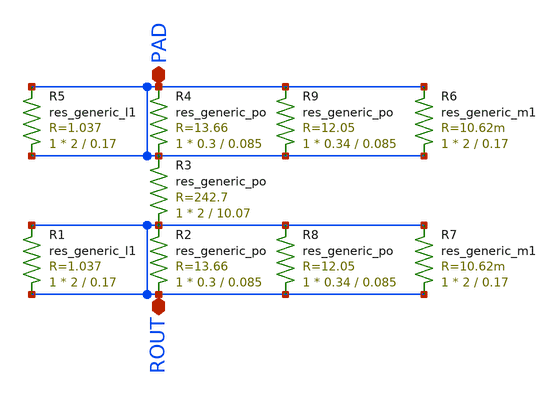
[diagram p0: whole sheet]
** sch_path: res250only_small.sch
* Copyright 2023 David Mitchell Bailey
* Licensed under the Apache License, Version 2.0 (the "License");
* you may not use this file except in compliance with the License.
* You may obtain a copy of the License at
* https://www.apache.org/licenses/LICENSE-2.0
* Unless required by applicable law or agreed to in writing, software
* distributed under the License is distributed on an "AS IS" BASIS,
* WITHOUT WARRANTIES OR CONDITIONS OF ANY KIND, either express or implied.
* See the License for the specific language governing permissions and
* limitations under the License.
**.subckt res250only_small PAD ROUT
*.iopin PAD
*.iopin ROUT
XR2 ROUT ROUT sky130_fd_pr__res_generic_po W=0.3 L=0.085 m=1
XR3 ROUT PAD sky130_fd_pr__res_generic_po W=2 L=10.07 m=1
XR4 PAD PAD sky130_fd_pr__res_generic_po W=0.3 L=0.085 m=1
R1 ROUT ROUT sky130_fd_pr__res_generic_l1 W=2 L=0.17 m=1
R5 PAD PAD sky130_fd_pr__res_generic_l1 W=2 L=0.17 m=1
R6 PAD PAD sky130_fd_pr__res_generic_m1 W=2 L=0.17 m=1
R7 ROUT ROUT sky130_fd_pr__res_generic_m1 W=2 L=0.17 m=1
XR8 ROUT ROUT sky130_fd_pr__res_generic_po W=0.34 L=0.085 m=1
XR9 PAD PAD sky130_fd_pr__res_generic_po W=0.34 L=0.085 m=1
**.ends
.end
